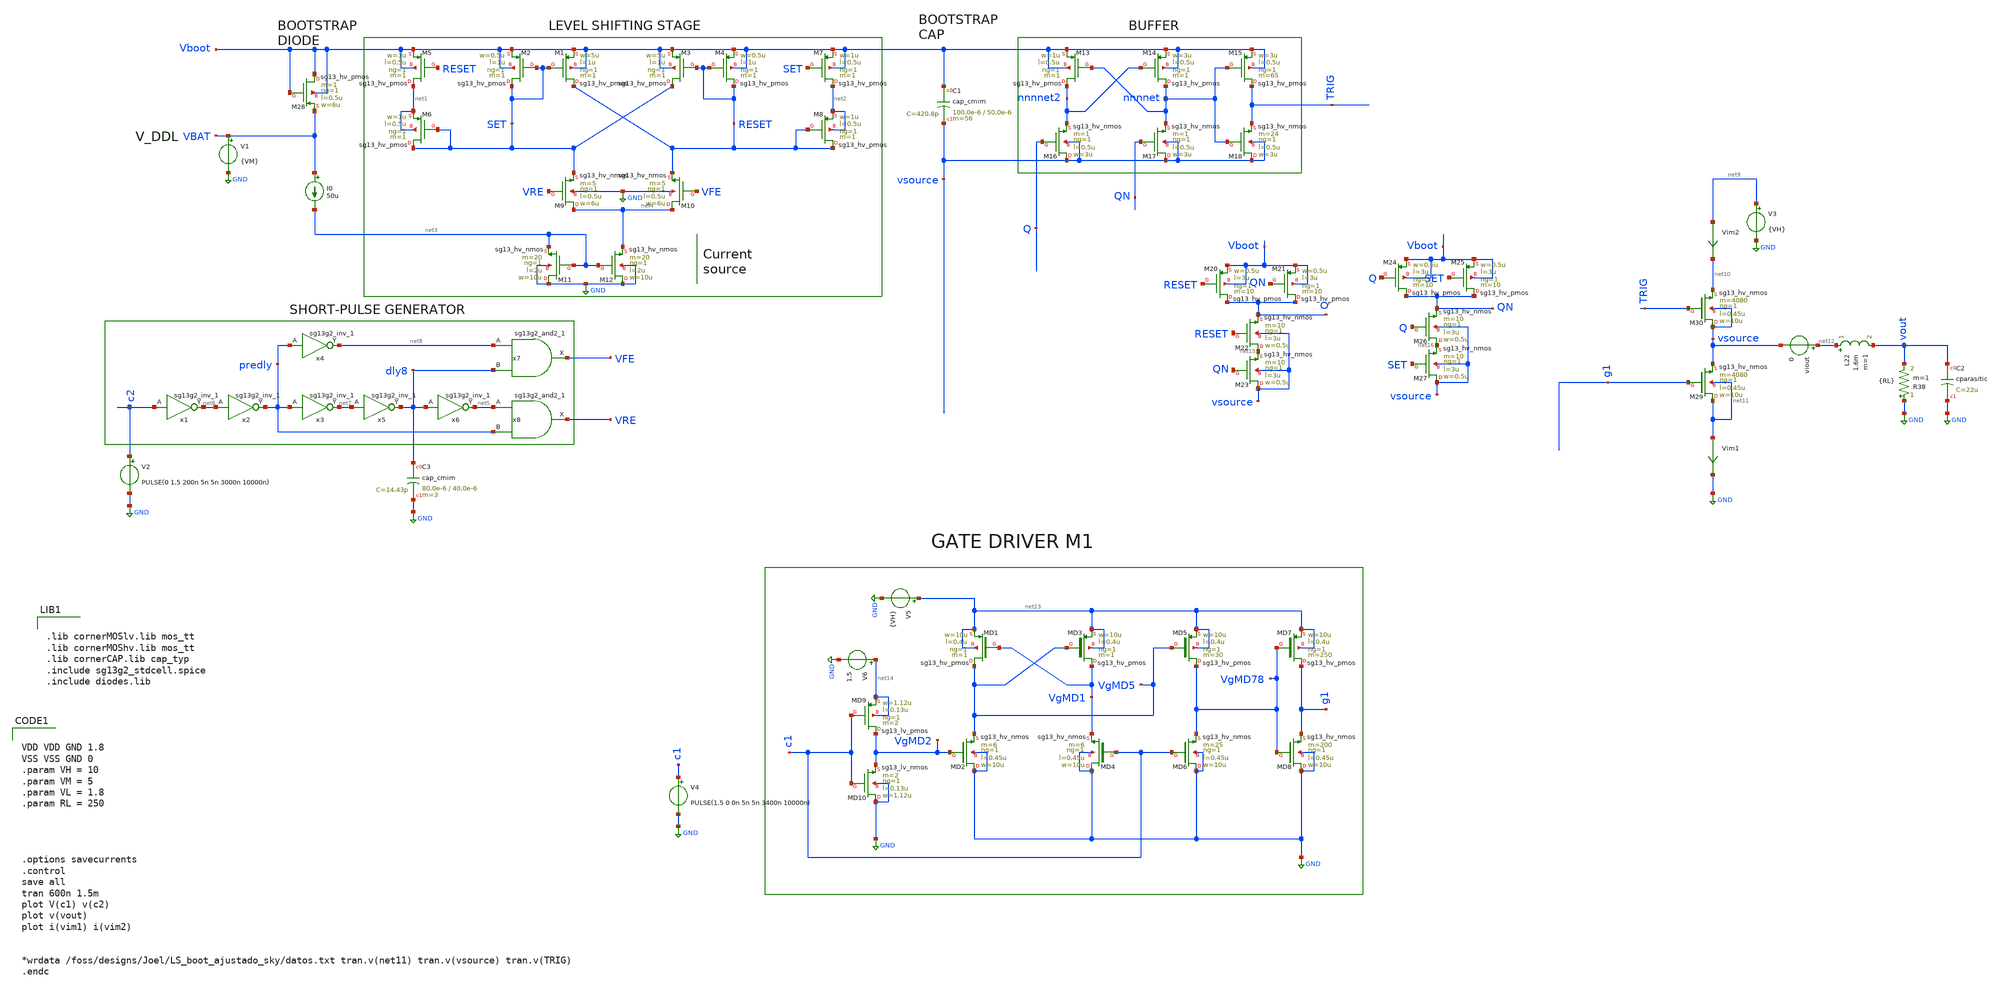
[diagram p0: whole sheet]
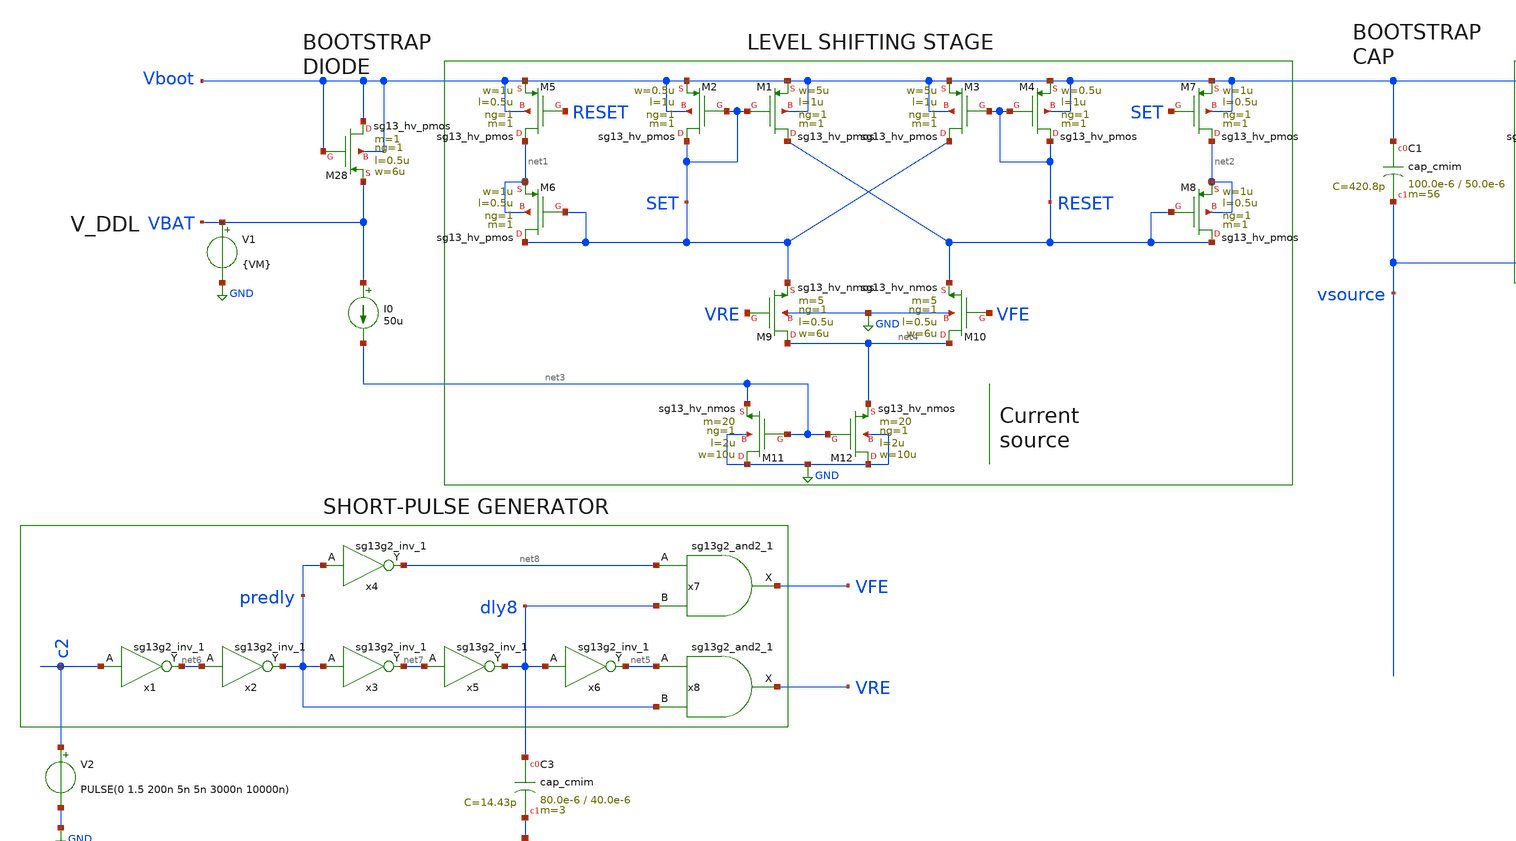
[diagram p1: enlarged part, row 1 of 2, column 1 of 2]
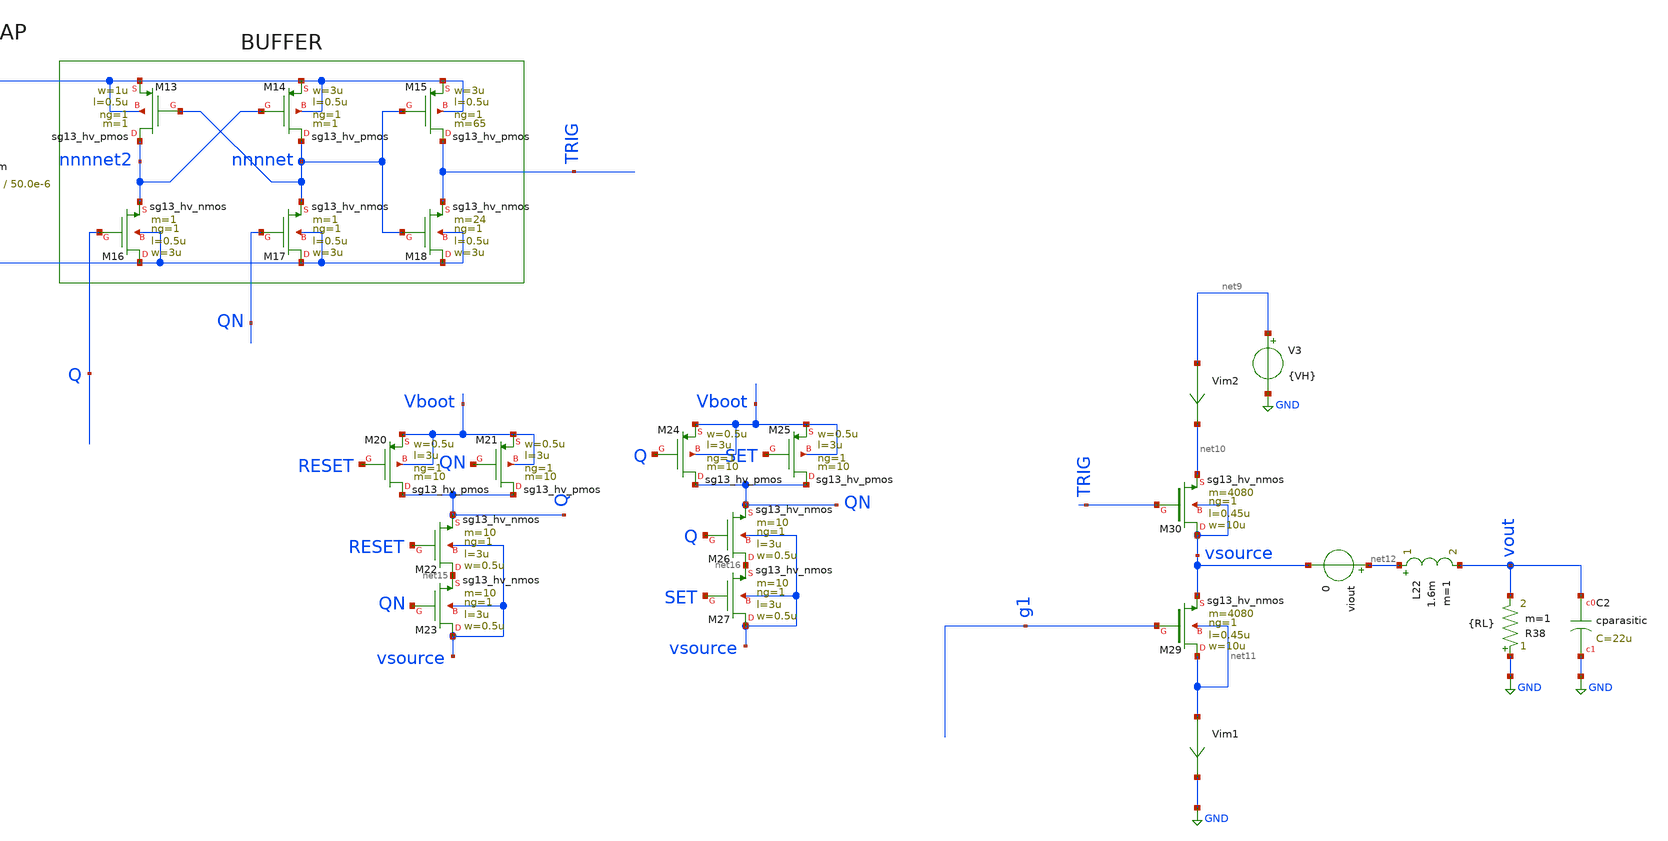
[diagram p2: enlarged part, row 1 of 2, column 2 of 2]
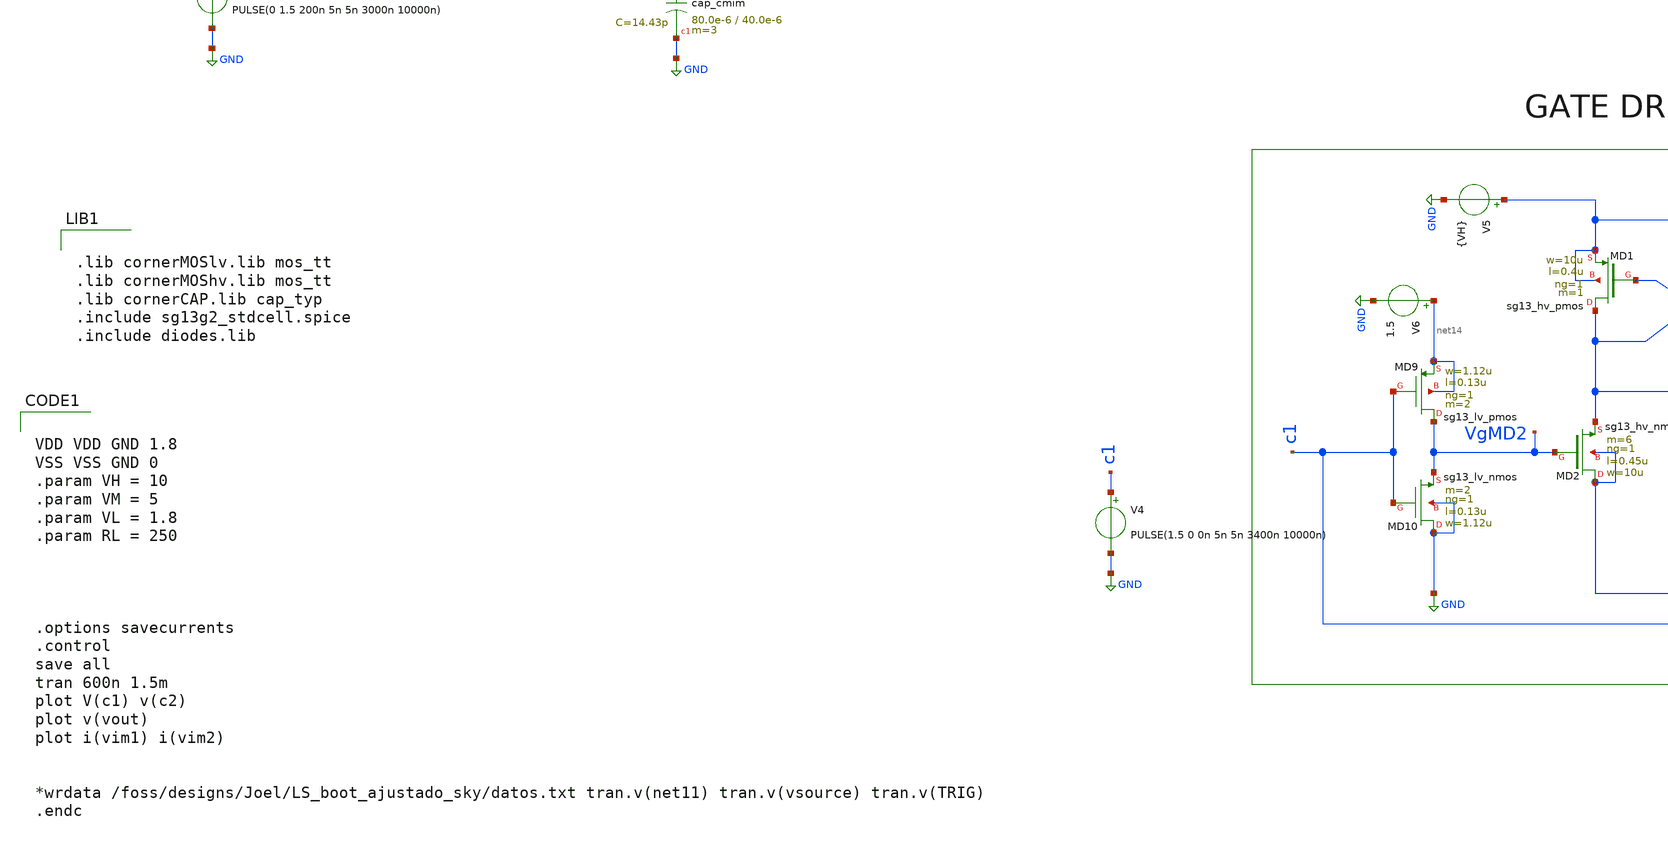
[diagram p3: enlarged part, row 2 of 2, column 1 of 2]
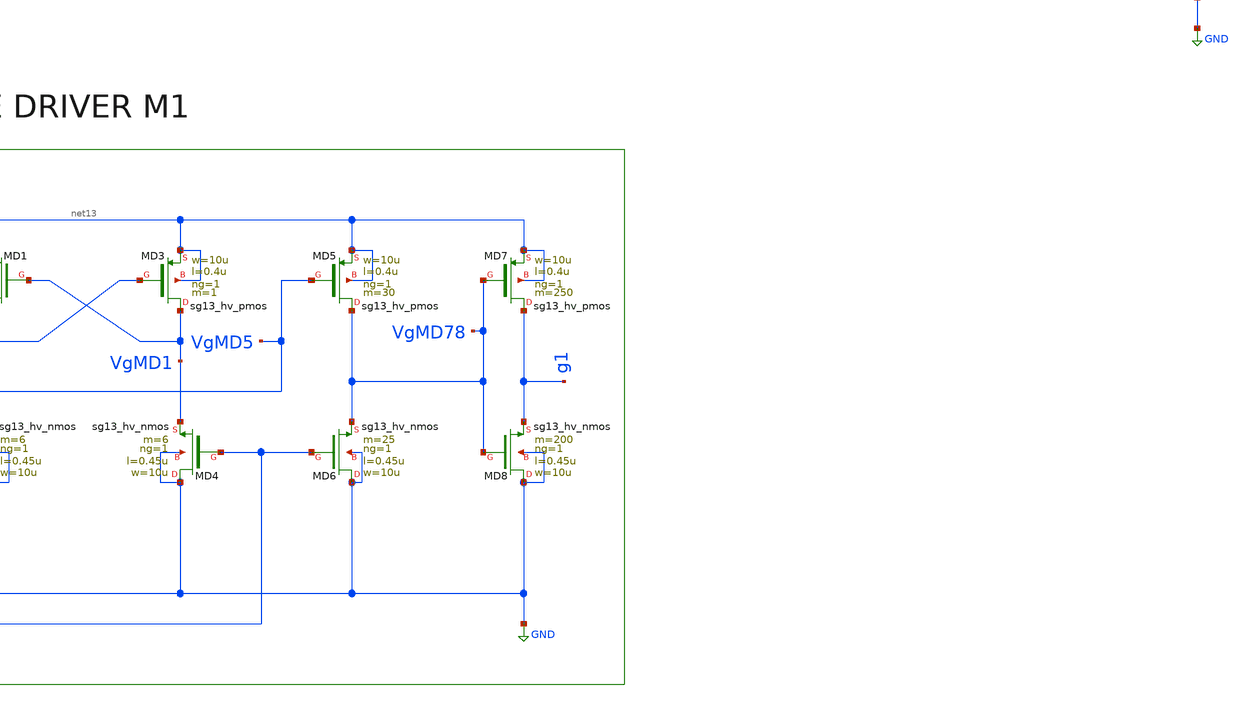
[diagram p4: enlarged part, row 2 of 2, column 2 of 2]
** sch_path: xschem/Simulation/Full_Sim1.sch
**.subckt Full_Sim1
V4 c1 GND PULSE(1.5 0 0n 5n 5n 3400n 10000n)
XM1 RESET SET Vboot Vboot sg13_hv_pmos w=5u l=1u ng=1 m=1 mm_ok=1
XM2 SET SET Vboot Vboot sg13_hv_pmos w=0.5u l=1u ng=1 m=1 mm_ok=1
XM3 SET RESET Vboot Vboot sg13_hv_pmos w=5u l=1u ng=1 m=1 mm_ok=1
XM4 RESET RESET Vboot Vboot sg13_hv_pmos w=0.5u l=1u ng=1 m=1 mm_ok=1
XM5 net1 RESET Vboot Vboot sg13_hv_pmos w=1u l=0.5u ng=1 m=1 mm_ok=1
XM6 SET SET net1 net1 sg13_hv_pmos w=1u l=0.5u ng=1 m=1 mm_ok=1
XM7 net2 SET Vboot Vboot sg13_hv_pmos w=1u l=0.5u ng=1 m=1 mm_ok=1
XM8 RESET RESET net2 net2 sg13_hv_pmos w=1u l=0.5u ng=1 m=1 mm_ok=1
XM9 net4 VRE SET GND sg13_hv_nmos w=6u l=0.5u ng=1 m=5 mm_ok=1
XM10 net4 VFE RESET GND sg13_hv_nmos w=6u l=0.5u ng=1 m=5 mm_ok=1
XM11 GND net3 net3 GND sg13_hv_nmos w=10u l=2u ng=1 m=20 mm_ok=1
XM12 GND net3 net4 GND sg13_hv_nmos w=10u l=2u ng=1 m=20 mm_ok=1
XM13 nnnnet2 nnnnet Vboot Vboot sg13_hv_pmos w=1u l=0.5u ng=1 m=1 mm_ok=1
XM14 nnnnet nnnnet2 Vboot Vboot sg13_hv_pmos w=3u l=0.5u ng=1 m=1 mm_ok=1
XM15 TRIG nnnnet Vboot Vboot sg13_hv_pmos w=3u l=0.5u ng=1 m=65 mm_ok=1
XM16 vsource Q nnnnet2 vsource sg13_hv_nmos w=3u l=0.5u ng=1 m=1 mm_ok=1
XM17 vsource QN nnnnet vsource sg13_hv_nmos w=3u l=0.5u ng=1 m=1 mm_ok=1
XM18 vsource nnnnet TRIG vsource sg13_hv_nmos w=3u l=0.5u ng=1 m=24 mm_ok=1
XM20 Q RESET Vboot Vboot sg13_hv_pmos w=0.5u l=3u ng=1 m=10 mm_ok=1
XM21 Q QN Vboot Vboot sg13_hv_pmos w=0.5u l=3u ng=1 m=10 mm_ok=1
XM22 net15 RESET Q vsource sg13_hv_nmos w=0.5u l=3u ng=1 m=10 mm_ok=1
XM23 vsource QN net15 vsource sg13_hv_nmos w=0.5u l=3u ng=1 m=10 mm_ok=1
XM24 QN Q Vboot Vboot sg13_hv_pmos w=0.5u l=3u ng=1 m=10 mm_ok=1
XM25 QN SET Vboot Vboot sg13_hv_pmos w=0.5u l=3u ng=1 m=10 mm_ok=1
XM26 net16 Q QN vsource sg13_hv_nmos w=0.5u l=3u ng=1 m=10 mm_ok=1
XM27 vsource SET net16 vsource sg13_hv_nmos w=0.5u l=3u ng=1 m=10 mm_ok=1
x1 net6 c2 VDD VSS sg13g2_inv_1
x2 predly net6 VDD VSS sg13g2_inv_1
x3 net7 predly VDD VSS sg13g2_inv_1
x4 net8 predly VDD VSS sg13g2_inv_1
x5 dly8 net7 VDD VSS sg13g2_inv_1
x6 net5 dly8 VDD VSS sg13g2_inv_1
XC1 Vboot vsource cap_cmim w=100.0e-6 l=50.0e-6 m=56 mm_ok=1
XM28 Vboot Vboot VBAT Vboot sg13_hv_pmos w=6u l=0.5u ng=1 m=1 mm_ok=1
XM30 vsource TRIG net10 vsource sg13_hv_nmos w=10u l=0.45u ng=1 m=4080 mm_ok=1
V3 net9 GND {VH}
x7 VFE net8 dly8 VDD VSS sg13g2_and2_1
x8 VRE net5 predly VDD VSS sg13g2_and2_1
Vim2 net9 net10 0
.save i(vim2)
R38 GND vout {RL} m=1
viout net12 vsource 0
XC3 dly8 GND cap_cmim w=80.0e-6 l=40.0e-6 m=3 mm_ok=1
XM29 net11 g1 vsource net11 sg13_hv_nmos w=10u l=0.45u ng=1 m=4080 mm_ok=1
Vim1 net11 GND 0
.save i(vim1)
L22 net12 vout 1.6m m=1
V2 c2 GND PULSE(0 1.5 200n 5n 5n 3000n 10000n)
XMD9 VgMD2 c1 net14 net14 sg13_lv_pmos w=1.12u l=0.13u ng=1 m=2 mm_ok=1
XMD10 GND c1 VgMD2 GND sg13_lv_nmos w=1.12u l=0.13u ng=1 m=2 mm_ok=1
XMD1 VgMD5 VgMD1 net13 net13 sg13_hv_pmos w=10u l=0.4u ng=1 m=1 mm_ok=1
XMD3 VgMD1 VgMD5 net13 net13 sg13_hv_pmos w=10u l=0.4u ng=1 m=1 mm_ok=1
XMD5 VgMD78 VgMD5 net13 net13 sg13_hv_pmos w=10u l=0.4u ng=1 m=30 mm_ok=1
XMD7 g1 VgMD78 net13 net13 sg13_hv_pmos w=10u l=0.4u ng=1 m=250 mm_ok=1
XMD2 GND VgMD2 VgMD5 GND sg13_hv_nmos w=10u l=0.45u ng=1 m=6 mm_ok=1
XMD4 GND c1 VgMD1 GND sg13_hv_nmos w=10u l=0.45u ng=1 m=6 mm_ok=1
XMD6 GND c1 VgMD78 GND sg13_hv_nmos w=10u l=0.45u ng=1 m=25 mm_ok=1
XMD8 GND VgMD78 g1 GND sg13_hv_nmos w=10u l=0.45u ng=1 m=200 mm_ok=1
V5 net13 GND {VH}
V6 net14 GND 1.5
XC2 vout GND cparasitic C=22u
I0 VBAT net3 50u
V1 VBAT GND {VM}
**** begin user architecture code


VDD VDD GND 1.8
VSS VSS GND 0
.param VH = 10
.param VM = 5
.param VL = 1.8
.param RL = 250




.options savecurrents
.control
save all
tran 600n 1.5m
plot V(c1) v(c2)
plot v(vout)
plot i(vim1) i(vim2)


*wrdata /foss/designs/Joel/LS_boot_ajustado_sky/datos.txt tran.v(net11) tran.v(vsource) tran.v(TRIG)
.endc




.lib cornerMOSlv.lib mos_tt
.lib cornerMOShv.lib mos_tt
.lib cornerCAP.lib cap_typ
.include sg13g2_stdcell.spice
.include diodes.lib


**** end user architecture code
**.ends

* expanding   symbol:  sg13g2_stdcells/sg13g2_inv_1.sym # of pins=2
** sym_path: sg13g2_stdcells/sg13g2_inv_1.sym
** sch_path: sg13g2_stdcells/sg13g2_inv_1.sch
.subckt sg13g2_inv_1 Y A VDD VSS
*.opin Y
*.ipin A
*.iopin VDD
*.iopin VSS
XM1 Y A VSS VSS sg13_lv_nmos w=740.00n l=130.00n ng=1 m=1 mm_ok=1
XM2 Y A VDD VDD sg13_lv_pmos w=1.12u l=130.00n ng=1 m=1 mm_ok=1
.ends


* expanding   symbol:  sg13g2_stdcells/sg13g2_and2_1.sym # of pins=3
** sym_path: sg13g2_stdcells/sg13g2_and2_1.sym
** sch_path: sg13g2_stdcells/sg13g2_and2_1.sch
.subckt sg13g2_and2_1 X A B VDD VSS
*.ipin A
*.ipin B
*.opin X
*.iopin VDD
*.iopin VSS
XM1 net1 A net2 VSS sg13_lv_nmos w=640.00n l=130.00n ng=1 m=1 mm_ok=1
XM2 net2 B VSS VSS sg13_lv_nmos w=640.00n l=130.00n ng=1 m=1 mm_ok=1
XM3 X net1 VSS VSS sg13_lv_nmos w=740.00n l=130.00n ng=1 m=1 mm_ok=1
XM4 net1 B VDD VDD sg13_lv_pmos w=840.00n l=130.00n ng=1 m=1 mm_ok=1
XM5 net1 A VDD VDD sg13_lv_pmos w=840.00n l=130.00n ng=1 m=1 mm_ok=1
XM6 X net1 VDD VDD sg13_lv_pmos w=1.12u l=130.00n ng=1 m=1 mm_ok=1
.ends

.GLOBAL GND
.end
